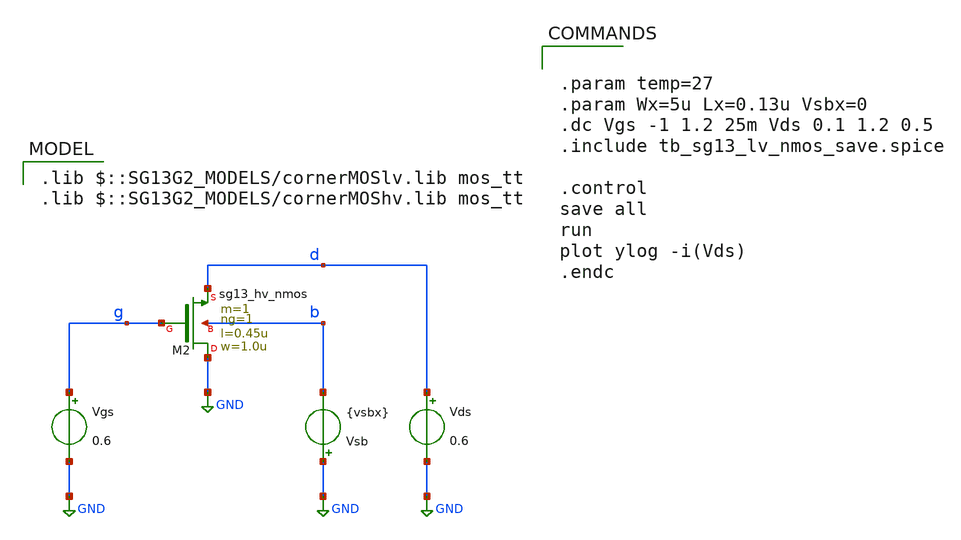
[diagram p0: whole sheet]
** sch_path: 4_Technology/src/tb_sg13_lv_nmos_gidl.sch
**.subckt tb_sg13_lv_nmos_gidl
Vgs g GND 0.6
Vds d GND 0.6
Vsb GND b {vsbx}
XM2 GND g d b sg13_hv_nmos w=1.0u l=0.45u ng=1 m=1 mm_ok=1
**** begin user architecture code
 .lib $::SG13G2_MODELS/cornerMOSlv.lib mos_tt
.lib $::SG13G2_MODELS/cornerMOShv.lib mos_tt



.param temp=27
.param Wx=5u Lx=0.13u Vsbx=0
.dc Vgs -1 1.2 25m Vds 0.1 1.2 0.5
.include tb_sg13_lv_nmos_save.spice

.control
save all
run
plot ylog -i(Vds)
.endc


**** end user architecture code
**.ends
.GLOBAL GND
.end
